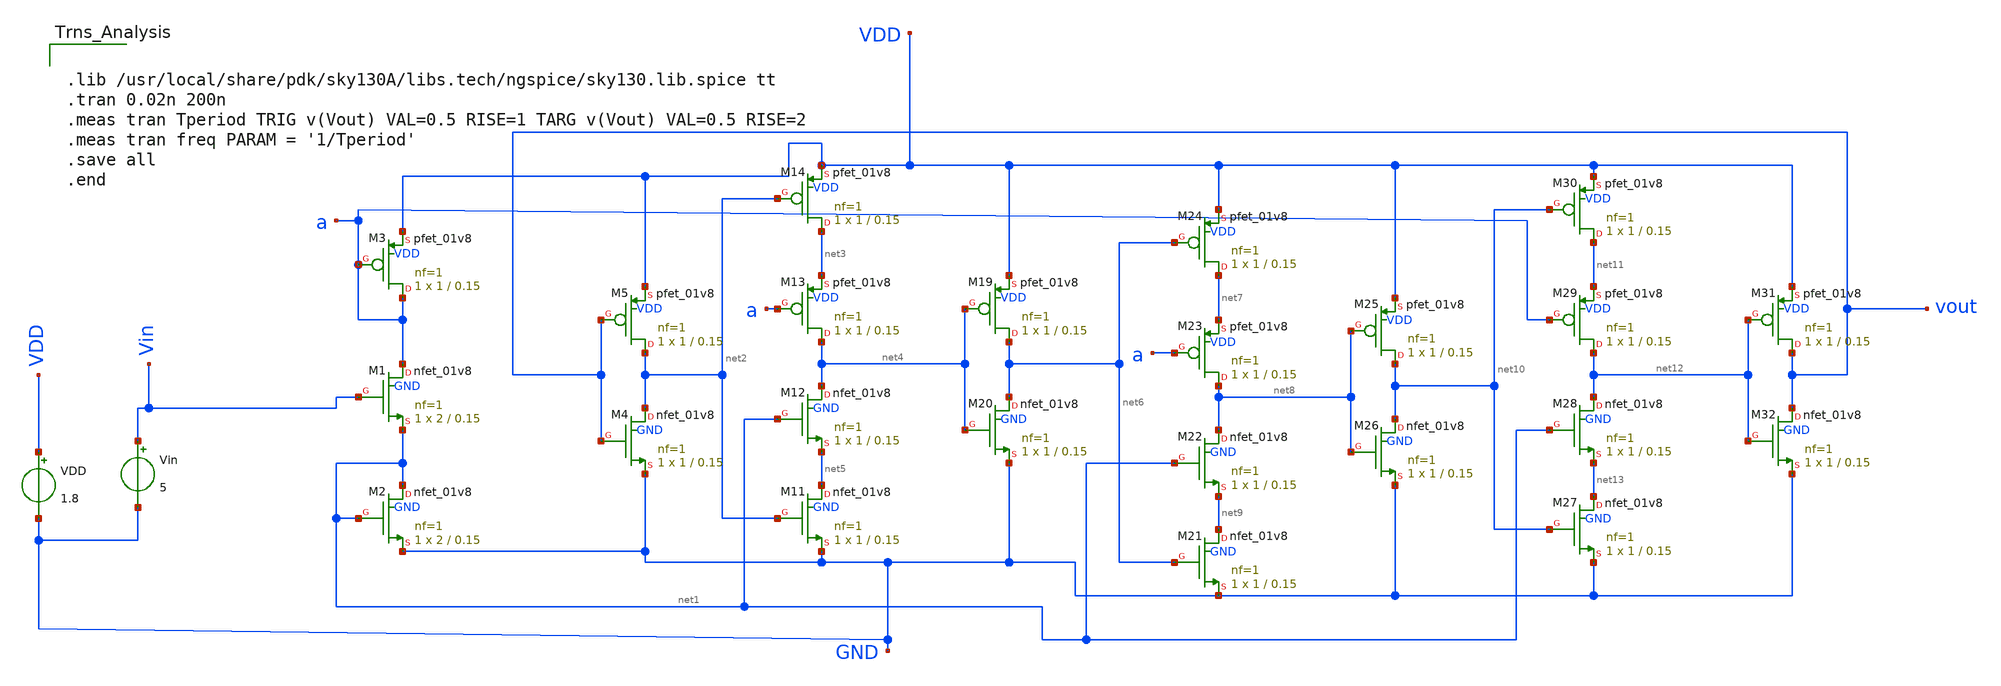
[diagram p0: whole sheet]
** sch_path: ros_ckt.sch
**.subckt ros_ckt
XM3 a a VDD VDD sky130_fd_pr__pfet_01v8 L=0.15 W=1 nf=1 ad='int((nf+1)/2) * W/nf * 0.29' as='int((nf+2)/2) * W/nf * 0.29'
+ pd='2*int((nf+1)/2) * (W/nf + 0.29)' ps='2*int((nf+2)/2) * (W/nf + 0.29)' nrd='0.29 / W' nrs='0.29 / W'
+ sa=0 sb=0 sd=0 mult=1 m=1
XM5 net2 vout VDD VDD sky130_fd_pr__pfet_01v8 L=0.15 W=1 nf=1 ad='int((nf+1)/2) * W/nf * 0.29' as='int((nf+2)/2) * W/nf * 0.29'
+ pd='2*int((nf+1)/2) * (W/nf + 0.29)' ps='2*int((nf+2)/2) * (W/nf + 0.29)' nrd='0.29 / W' nrs='0.29 / W'
+ sa=0 sb=0 sd=0 mult=1 m=1
XM1 a Vin net1 GND sky130_fd_pr__nfet_01v8 L=0.15 W=2 nf=1 ad='int((nf+1)/2) * W/nf * 0.29' as='int((nf+2)/2) * W/nf * 0.29'
+ pd='2*int((nf+1)/2) * (W/nf + 0.29)' ps='2*int((nf+2)/2) * (W/nf + 0.29)' nrd='0.29 / W' nrs='0.29 / W'
+ sa=0 sb=0 sd=0 mult=1 m=1
XM2 net1 net1 GND GND sky130_fd_pr__nfet_01v8 L=0.15 W=2 nf=1 ad='int((nf+1)/2) * W/nf * 0.29' as='int((nf+2)/2) * W/nf * 0.29'
+ pd='2*int((nf+1)/2) * (W/nf + 0.29)' ps='2*int((nf+2)/2) * (W/nf + 0.29)' nrd='0.29 / W' nrs='0.29 / W'
+ sa=0 sb=0 sd=0 mult=1 m=1
XM4 net2 vout GND GND sky130_fd_pr__nfet_01v8 L=0.15 W=1 nf=1 ad='int((nf+1)/2) * W/nf * 0.29' as='int((nf+2)/2) * W/nf * 0.29'
+ pd='2*int((nf+1)/2) * (W/nf + 0.29)' ps='2*int((nf+2)/2) * (W/nf + 0.29)' nrd='0.29 / W' nrs='0.29 / W'
+ sa=0 sb=0 sd=0 mult=1 m=1
XM11 net5 net2 GND GND sky130_fd_pr__nfet_01v8 L=0.15 W=1 nf=1 ad='int((nf+1)/2) * W/nf * 0.29' as='int((nf+2)/2) * W/nf * 0.29'
+ pd='2*int((nf+1)/2) * (W/nf + 0.29)' ps='2*int((nf+2)/2) * (W/nf + 0.29)' nrd='0.29 / W' nrs='0.29 / W'
+ sa=0 sb=0 sd=0 mult=1 m=1
XM12 net4 net1 net5 GND sky130_fd_pr__nfet_01v8 L=0.15 W=1 nf=1 ad='int((nf+1)/2) * W/nf * 0.29' as='int((nf+2)/2) * W/nf * 0.29'
+ pd='2*int((nf+1)/2) * (W/nf + 0.29)' ps='2*int((nf+2)/2) * (W/nf + 0.29)' nrd='0.29 / W' nrs='0.29 / W'
+ sa=0 sb=0 sd=0 mult=1 m=1
XM13 net4 a net3 VDD sky130_fd_pr__pfet_01v8 L=0.15 W=1 nf=1 ad='int((nf+1)/2) * W/nf * 0.29' as='int((nf+2)/2) * W/nf * 0.29'
+ pd='2*int((nf+1)/2) * (W/nf + 0.29)' ps='2*int((nf+2)/2) * (W/nf + 0.29)' nrd='0.29 / W' nrs='0.29 / W'
+ sa=0 sb=0 sd=0 mult=1 m=1
XM14 net3 net2 VDD VDD sky130_fd_pr__pfet_01v8 L=0.15 W=1 nf=1 ad='int((nf+1)/2) * W/nf * 0.29' as='int((nf+2)/2) * W/nf * 0.29'
+ pd='2*int((nf+1)/2) * (W/nf + 0.29)' ps='2*int((nf+2)/2) * (W/nf + 0.29)' nrd='0.29 / W' nrs='0.29 / W'
+ sa=0 sb=0 sd=0 mult=1 m=1
XM19 net6 net4 VDD VDD sky130_fd_pr__pfet_01v8 L=0.15 W=1 nf=1 ad='int((nf+1)/2) * W/nf * 0.29' as='int((nf+2)/2) * W/nf * 0.29'
+ pd='2*int((nf+1)/2) * (W/nf + 0.29)' ps='2*int((nf+2)/2) * (W/nf + 0.29)' nrd='0.29 / W' nrs='0.29 / W'
+ sa=0 sb=0 sd=0 mult=1 m=1
XM20 net6 net4 GND GND sky130_fd_pr__nfet_01v8 L=0.15 W=1 nf=1 ad='int((nf+1)/2) * W/nf * 0.29' as='int((nf+2)/2) * W/nf * 0.29'
+ pd='2*int((nf+1)/2) * (W/nf + 0.29)' ps='2*int((nf+2)/2) * (W/nf + 0.29)' nrd='0.29 / W' nrs='0.29 / W'
+ sa=0 sb=0 sd=0 mult=1 m=1
XM21 net9 net6 GND GND sky130_fd_pr__nfet_01v8 L=0.15 W=1 nf=1 ad='int((nf+1)/2) * W/nf * 0.29' as='int((nf+2)/2) * W/nf * 0.29'
+ pd='2*int((nf+1)/2) * (W/nf + 0.29)' ps='2*int((nf+2)/2) * (W/nf + 0.29)' nrd='0.29 / W' nrs='0.29 / W'
+ sa=0 sb=0 sd=0 mult=1 m=1
XM22 net8 net1 net9 GND sky130_fd_pr__nfet_01v8 L=0.15 W=1 nf=1 ad='int((nf+1)/2) * W/nf * 0.29' as='int((nf+2)/2) * W/nf * 0.29'
+ pd='2*int((nf+1)/2) * (W/nf + 0.29)' ps='2*int((nf+2)/2) * (W/nf + 0.29)' nrd='0.29 / W' nrs='0.29 / W'
+ sa=0 sb=0 sd=0 mult=1 m=1
XM23 net8 a net7 VDD sky130_fd_pr__pfet_01v8 L=0.15 W=1 nf=1 ad='int((nf+1)/2) * W/nf * 0.29' as='int((nf+2)/2) * W/nf * 0.29'
+ pd='2*int((nf+1)/2) * (W/nf + 0.29)' ps='2*int((nf+2)/2) * (W/nf + 0.29)' nrd='0.29 / W' nrs='0.29 / W'
+ sa=0 sb=0 sd=0 mult=1 m=1
XM24 net7 net6 VDD VDD sky130_fd_pr__pfet_01v8 L=0.15 W=1 nf=1 ad='int((nf+1)/2) * W/nf * 0.29' as='int((nf+2)/2) * W/nf * 0.29'
+ pd='2*int((nf+1)/2) * (W/nf + 0.29)' ps='2*int((nf+2)/2) * (W/nf + 0.29)' nrd='0.29 / W' nrs='0.29 / W'
+ sa=0 sb=0 sd=0 mult=1 m=1
XM25 net10 net8 VDD VDD sky130_fd_pr__pfet_01v8 L=0.15 W=1 nf=1 ad='int((nf+1)/2) * W/nf * 0.29' as='int((nf+2)/2) * W/nf * 0.29'
+ pd='2*int((nf+1)/2) * (W/nf + 0.29)' ps='2*int((nf+2)/2) * (W/nf + 0.29)' nrd='0.29 / W' nrs='0.29 / W'
+ sa=0 sb=0 sd=0 mult=1 m=1
XM26 net10 net8 GND GND sky130_fd_pr__nfet_01v8 L=0.15 W=1 nf=1 ad='int((nf+1)/2) * W/nf * 0.29' as='int((nf+2)/2) * W/nf * 0.29'
+ pd='2*int((nf+1)/2) * (W/nf + 0.29)' ps='2*int((nf+2)/2) * (W/nf + 0.29)' nrd='0.29 / W' nrs='0.29 / W'
+ sa=0 sb=0 sd=0 mult=1 m=1
XM27 net13 net10 GND GND sky130_fd_pr__nfet_01v8 L=0.15 W=1 nf=1 ad='int((nf+1)/2) * W/nf * 0.29' as='int((nf+2)/2) * W/nf * 0.29'
+ pd='2*int((nf+1)/2) * (W/nf + 0.29)' ps='2*int((nf+2)/2) * (W/nf + 0.29)' nrd='0.29 / W' nrs='0.29 / W'
+ sa=0 sb=0 sd=0 mult=1 m=1
XM28 net12 net1 net13 GND sky130_fd_pr__nfet_01v8 L=0.15 W=1 nf=1 ad='int((nf+1)/2) * W/nf * 0.29' as='int((nf+2)/2) * W/nf * 0.29'
+ pd='2*int((nf+1)/2) * (W/nf + 0.29)' ps='2*int((nf+2)/2) * (W/nf + 0.29)' nrd='0.29 / W' nrs='0.29 / W'
+ sa=0 sb=0 sd=0 mult=1 m=1
XM29 net12 a net11 VDD sky130_fd_pr__pfet_01v8 L=0.15 W=1 nf=1 ad='int((nf+1)/2) * W/nf * 0.29' as='int((nf+2)/2) * W/nf * 0.29'
+ pd='2*int((nf+1)/2) * (W/nf + 0.29)' ps='2*int((nf+2)/2) * (W/nf + 0.29)' nrd='0.29 / W' nrs='0.29 / W'
+ sa=0 sb=0 sd=0 mult=1 m=1
XM30 net11 net10 VDD VDD sky130_fd_pr__pfet_01v8 L=0.15 W=1 nf=1 ad='int((nf+1)/2) * W/nf * 0.29' as='int((nf+2)/2) * W/nf * 0.29'
+ pd='2*int((nf+1)/2) * (W/nf + 0.29)' ps='2*int((nf+2)/2) * (W/nf + 0.29)' nrd='0.29 / W' nrs='0.29 / W'
+ sa=0 sb=0 sd=0 mult=1 m=1
XM31 vout net12 VDD VDD sky130_fd_pr__pfet_01v8 L=0.15 W=1 nf=1 ad='int((nf+1)/2) * W/nf * 0.29' as='int((nf+2)/2) * W/nf * 0.29'
+ pd='2*int((nf+1)/2) * (W/nf + 0.29)' ps='2*int((nf+2)/2) * (W/nf + 0.29)' nrd='0.29 / W' nrs='0.29 / W'
+ sa=0 sb=0 sd=0 mult=1 m=1
XM32 vout net12 GND GND sky130_fd_pr__nfet_01v8 L=0.15 W=1 nf=1 ad='int((nf+1)/2) * W/nf * 0.29' as='int((nf+2)/2) * W/nf * 0.29'
+ pd='2*int((nf+1)/2) * (W/nf + 0.29)' ps='2*int((nf+2)/2) * (W/nf + 0.29)' nrd='0.29 / W' nrs='0.29 / W'
+ sa=0 sb=0 sd=0 mult=1 m=1
Vin Vin GND 5
VDD VDD GND 1.8
**** begin user architecture code


.lib /usr/local/share/pdk/sky130A/libs.tech/ngspice/sky130.lib.spice tt
.tran 0.02n 200n
.meas tran Tperiod TRIG v(Vout) VAL=0.5 RISE=1 TARG v(Vout) VAL=0.5 RISE=2
.meas tran freq PARAM = '1/Tperiod'
.save all
.end

**** end user architecture code
**.ends
.end
